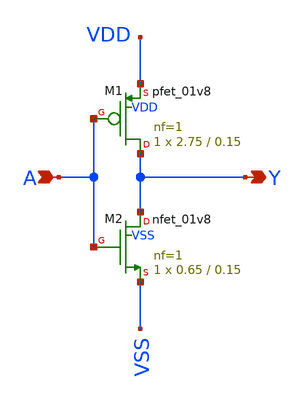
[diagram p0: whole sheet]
** sch_path: design/xschem/INV/inv_smol.sch
**.subckt inv_smol A Y
*.ipin A
*.opin Y
XM2 Y A VSS VSS sky130_fd_pr__nfet_01v8 L=0.15 W=0.65 nf=1 ad='int((nf+1)/2) * W/nf * 0.29' as='int((nf+2)/2) * W/nf * 0.29'
+ pd='2*int((nf+1)/2) * (W/nf + 0.29)' ps='2*int((nf+2)/2) * (W/nf + 0.29)' nrd='0.29 / W' nrs='0.29 / W'
+ sa=0 sb=0 sd=0 mult=1 m=1
XM1 Y A VDD VDD sky130_fd_pr__pfet_01v8 L=0.15 W=2.75 nf=1 ad='int((nf+1)/2) * W/nf * 0.29' as='int((nf+2)/2) * W/nf * 0.29'
+ pd='2*int((nf+1)/2) * (W/nf + 0.29)' ps='2*int((nf+2)/2) * (W/nf + 0.29)' nrd='0.29 / W' nrs='0.29 / W'
+ sa=0 sb=0 sd=0 mult=1 m=1
**.ends
.end
